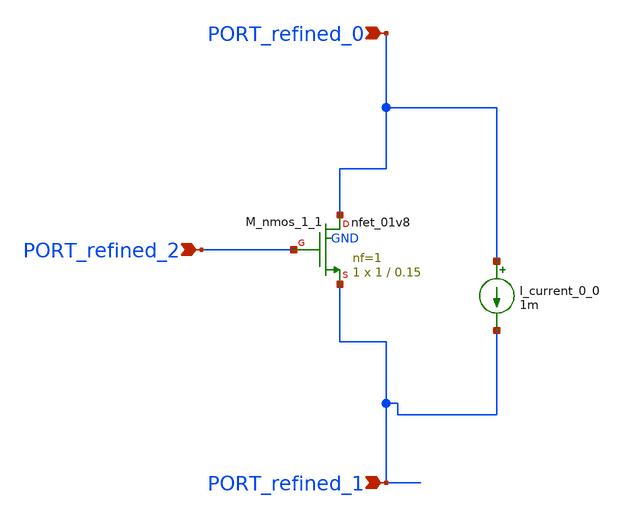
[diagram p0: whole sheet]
** sch_path: schematics/AMSNet/433.sch
**.subckt 433 PORT_refined_0 PORT_refined_2 PORT_refined_1
*.ipin PORT_refined_0
*.ipin PORT_refined_2
*.ipin PORT_refined_1
I_current_0_0 PORT_refined_0 PORT_refined_1 1m
XM_nmos_1_1 PORT_refined_0 PORT_refined_2 PORT_refined_1 GND sky130_fd_pr__nfet_01v8 L=0.15 W=1 nf=1
+ ad='int((1 + 1)/2) * 1 / 1 * 0.29' as='int((1 + 2)/2) * 1 / 1 * 0.29' pd='2*int((1 + 1)/2) * (1 / 1 + 0.29)'
+ ps='2*int((1 + 2)/2) * (1 / 1 + 0.29)' nrd='0.29 / 1 ' nrs='0.29 / 1 ' sa=0 sb=0 sd=0 mult=1 m=1
**.ends
.end
